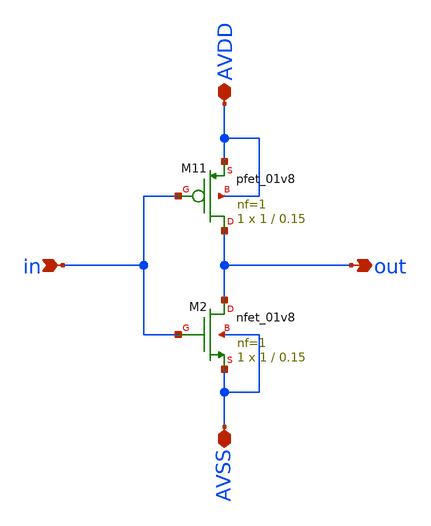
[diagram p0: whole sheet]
** sch_path: xschem/inverter.sch
**.subckt inverter out in AVSS AVDD
*.opin out
*.ipin in
*.iopin AVSS
*.iopin AVDD
XM11 out in AVDD AVDD sky130_fd_pr__pfet_01v8 L=0.15 W=1 nf=1 ad='int((nf+1)/2) * W/nf * 0.29' as='int((nf+2)/2) * W/nf * 0.29'
+ pd='2*int((nf+1)/2) * (W/nf + 0.29)' ps='2*int((nf+2)/2) * (W/nf + 0.29)' nrd='0.29 / W' nrs='0.29 / W'
+ sa=0 sb=0 sd=0 mult=1 m=1
XM2 out in AVSS AVSS sky130_fd_pr__nfet_01v8 L=0.15 W=1 nf=1 ad='int((1 + 1)/2) * 1 / 1 * 0.29' as='int((1 + 2)/2) * 1 / 1 * 0.29'
+ pd='2*int((1 + 1)/2) * (1 / 1 + 0.29)' ps='2*int((1 + 2)/2) * (1 / 1 + 0.29)' nrd='0.29 / 1 ' nrs='0.29 / 1 '
+ sa=0 sb=0 sd=0 mult=1 m=1
**.ends
.end
